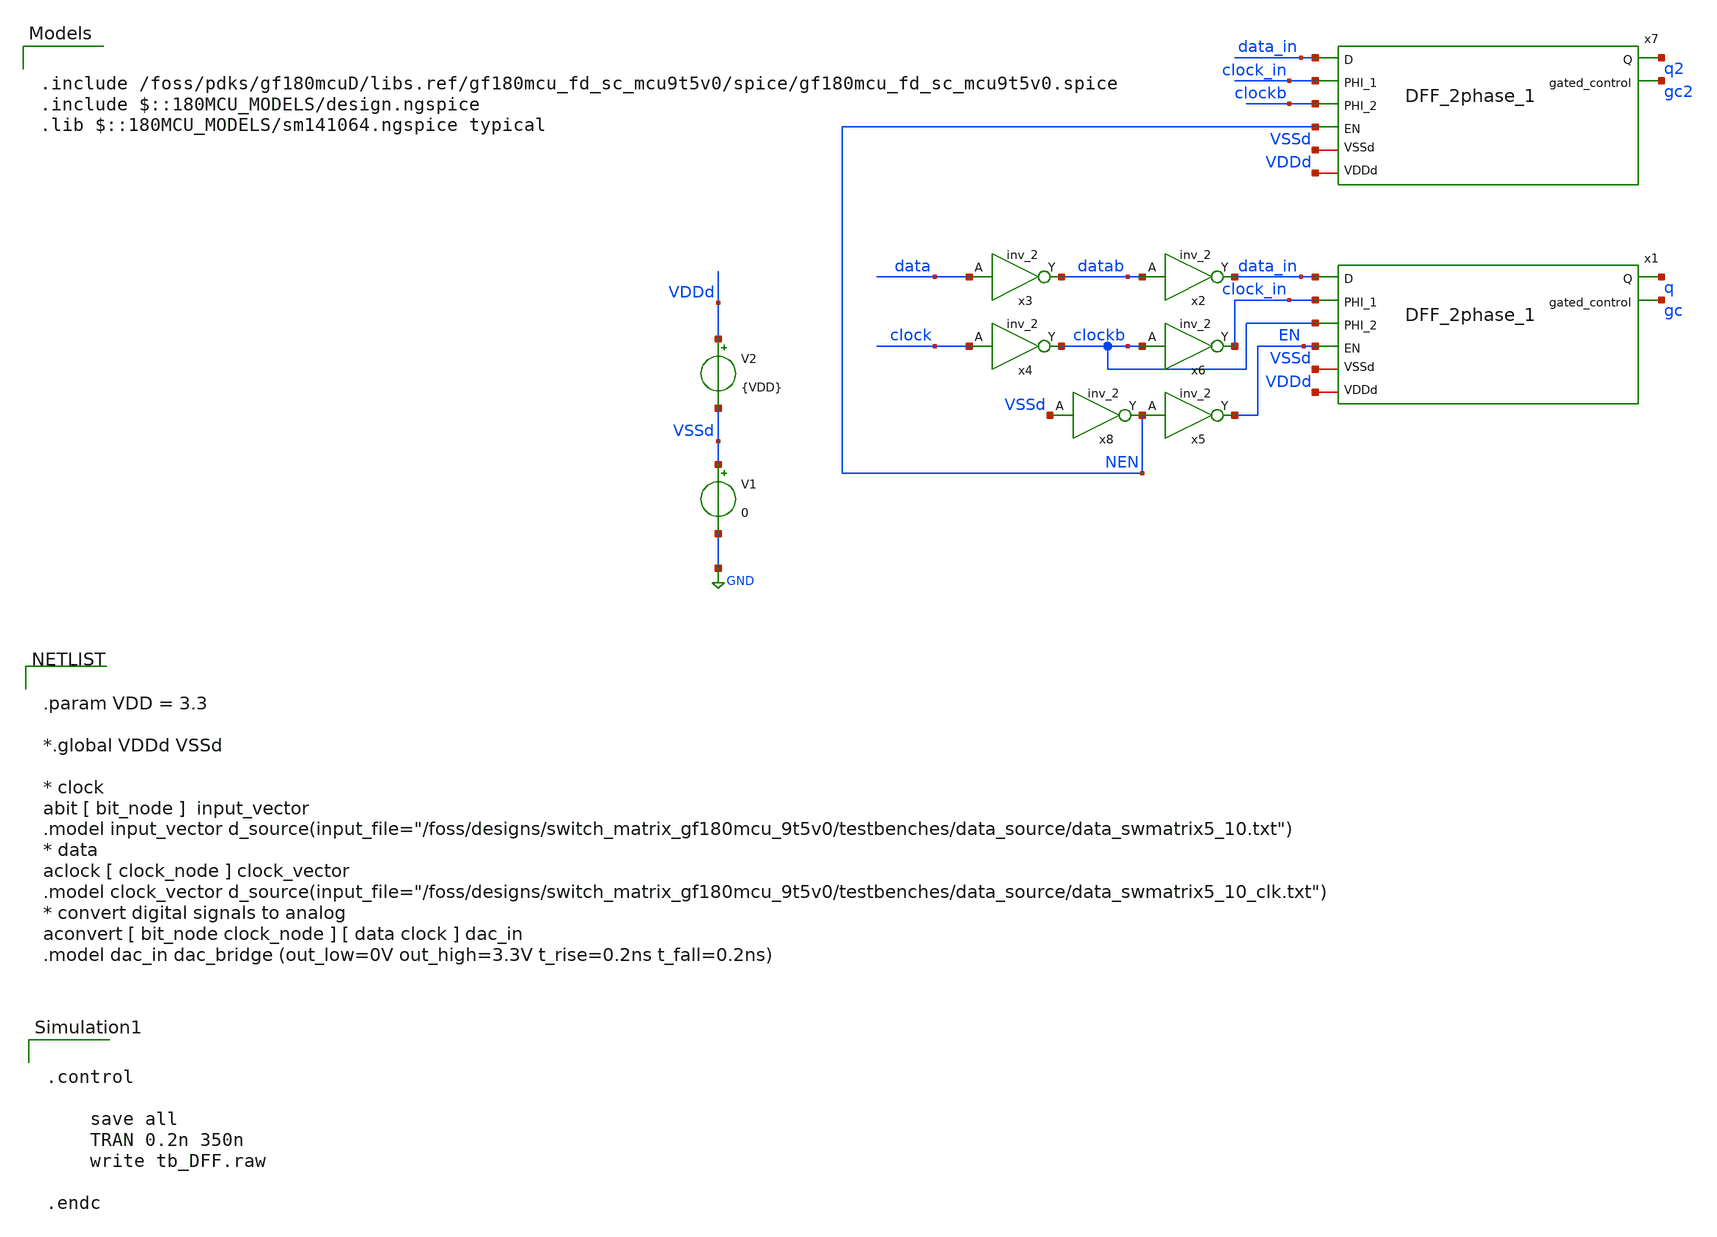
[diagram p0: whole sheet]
** sch_path: testbenches/tb_varioues/tb_DFF.sch
**.subckt tb_DFF
x1 q data_in clock_in gc clockb EN VDDd VSSd DFF_2phase_1
V1 VSSd GND 0
V2 VDDd VSSd {VDD}
x3 data VSSd VDDd VSSd VDDd datab gf180mcu_fd_sc_mcu9t5v0__inv_2
x2 datab VSSd VDDd VSSd VDDd data_in gf180mcu_fd_sc_mcu9t5v0__inv_2
x4 clock VSSd VDDd VSSd VDDd clockb gf180mcu_fd_sc_mcu9t5v0__inv_2
x5 NEN VSSd VDDd VSSd VDDd EN gf180mcu_fd_sc_mcu9t5v0__inv_2
x6 clockb VSSd VDDd VSSd VDDd clock_in gf180mcu_fd_sc_mcu9t5v0__inv_2
x7 q2 data_in clock_in gc2 clockb NEN VDDd VSSd DFF_2phase_1
x8 VSSd VSSd VDDd VSSd VDDd NEN gf180mcu_fd_sc_mcu9t5v0__inv_2
**** begin user architecture code

.include /foss/pdks/gf180mcuD/libs.ref/gf180mcu_fd_sc_mcu9t5v0/spice/gf180mcu_fd_sc_mcu9t5v0.spice
.include $::180MCU_MODELS/design.ngspice
.lib $::180MCU_MODELS/sm141064.ngspice typical



.param VDD = 3.3

*.global VDDd VSSd

* clock
abit [ bit_node ]  input_vector
.model input_vector
+ d_source(input_file="/foss/designs/switch_matrix_gf180mcu_9t5v0/testbenches/data_source/data_swmatrix5_10.txt")
* data
aclock [ clock_node ] clock_vector
.model clock_vector
+ d_source(input_file="/foss/designs/switch_matrix_gf180mcu_9t5v0/testbenches/data_source/data_swmatrix5_10_clk.txt")
* convert digital signals to analog
aconvert [ bit_node clock_node ] [ data clock ] dac_in
.model dac_in dac_bridge (out_low=0V out_high=3.3V t_rise=0.2ns t_fall=0.2ns)




.control

    save all
    TRAN 0.2n 350n
    write tb_DFF.raw

.endc


**** end user architecture code
**.ends
.GLOBAL GND
.end
